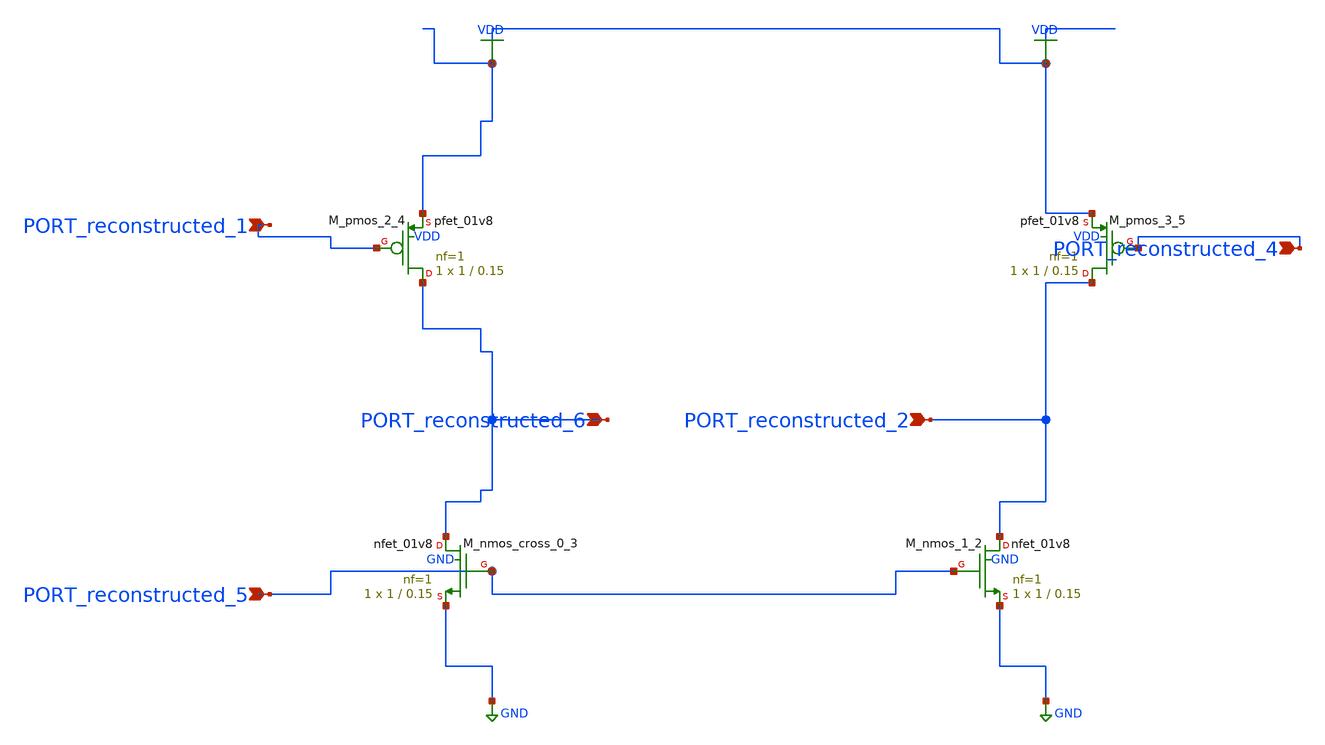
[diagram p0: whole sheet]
** sch_path: schematics/AMSNet/715.sch
**.subckt 715 PORT_reconstructed_1 PORT_reconstructed_2 PORT_reconstructed_5 PORT_reconstructed_6
*+ PORT_reconstructed_4
*.ipin PORT_reconstructed_1
*.ipin PORT_reconstructed_2
*.ipin PORT_reconstructed_5
*.ipin PORT_reconstructed_6
*.ipin PORT_reconstructed_4
XM_nmos_1_2 PORT_reconstructed_2 PORT_reconstructed_5 GND GND sky130_fd_pr__nfet_01v8 L=0.15 W=1 nf=1
+ ad='int((1 + 1)/2) * 1 / 1 * 0.29' as='int((1 + 2)/2) * 1 / 1 * 0.29' pd='2*int((1 + 1)/2) * (1 / 1 + 0.29)'
+ ps='2*int((1 + 2)/2) * (1 / 1 + 0.29)' nrd='0.29 / 1 ' nrs='0.29 / 1 ' sa=0 sb=0 sd=0 mult=1 m=1
XM_nmos_cross_0_3 PORT_reconstructed_6 PORT_reconstructed_5 GND GND sky130_fd_pr__nfet_01v8 L=0.15 W=1
+ nf=1 ad='int((1 + 1)/2) * 1 / 1 * 0.29' as='int((1 + 2)/2) * 1 / 1 * 0.29' pd='2*int((1 + 1)/2) * (1 / 1 + 0.29)'
+ ps='2*int((1 + 2)/2) * (1 / 1 + 0.29)' nrd='0.29 / 1 ' nrs='0.29 / 1 ' sa=0 sb=0 sd=0 mult=1 m=1
XM_pmos_2_4 PORT_reconstructed_6 PORT_reconstructed_1 VDD VDD sky130_fd_pr__pfet_01v8 L=0.15 W=1 nf=1
+ ad='int((1 + 1)/2) * 1 / 1 * 0.29' as='int((1 + 2)/2) * 1 / 1 * 0.29' pd='2*int((1 + 1)/2) * (1 / 1 + 0.29)'
+ ps='2*int((1 + 2)/2) * (1 / 1 + 0.29)' nrd='0.29 / 1 ' nrs='0.29 / 1 ' sa=0 sb=0 sd=0 mult=1 m=1
XM_pmos_3_5 PORT_reconstructed_2 PORT_reconstructed_4 VDD VDD sky130_fd_pr__pfet_01v8 L=0.15 W=1 nf=1
+ ad='int((1 + 1)/2) * 1 / 1 * 0.29' as='int((1 + 2)/2) * 1 / 1 * 0.29' pd='2*int((1 + 1)/2) * (1 / 1 + 0.29)'
+ ps='2*int((1 + 2)/2) * (1 / 1 + 0.29)' nrd='0.29 / 1 ' nrs='0.29 / 1 ' sa=0 sb=0 sd=0 mult=1 m=1
**.ends
.GLOBAL GND
.GLOBAL VDD
.end
